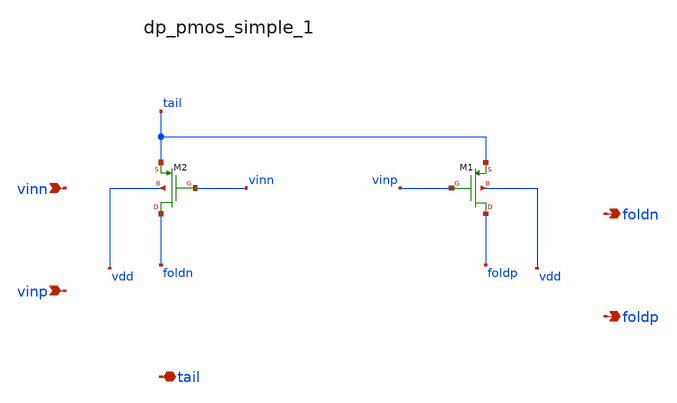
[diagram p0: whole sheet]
** sch_path: analog-db/raw/amp_004_folded_cascode/hier/blocks/dp_pmos_simple_1.sch
**.subckt dp_pmos_simple_1 vinn vinp tail foldn foldp
*.ipin vinn
*.ipin vinp
*.iopin tail
*.opin foldn
*.opin foldp
XM1 foldp vinp tail vdd sg13_lv_pmos w=x_dut_xm1_w l=x_dut_xm1_l ng=x_dut_xm1_ng m=x_dut_xm1_m
XM2 foldn vinn tail vdd sg13_lv_pmos w=x_dut_xm2_w l=x_dut_xm2_l ng=x_dut_xm2_ng m=x_dut_xm2_m
**.ends
.end
